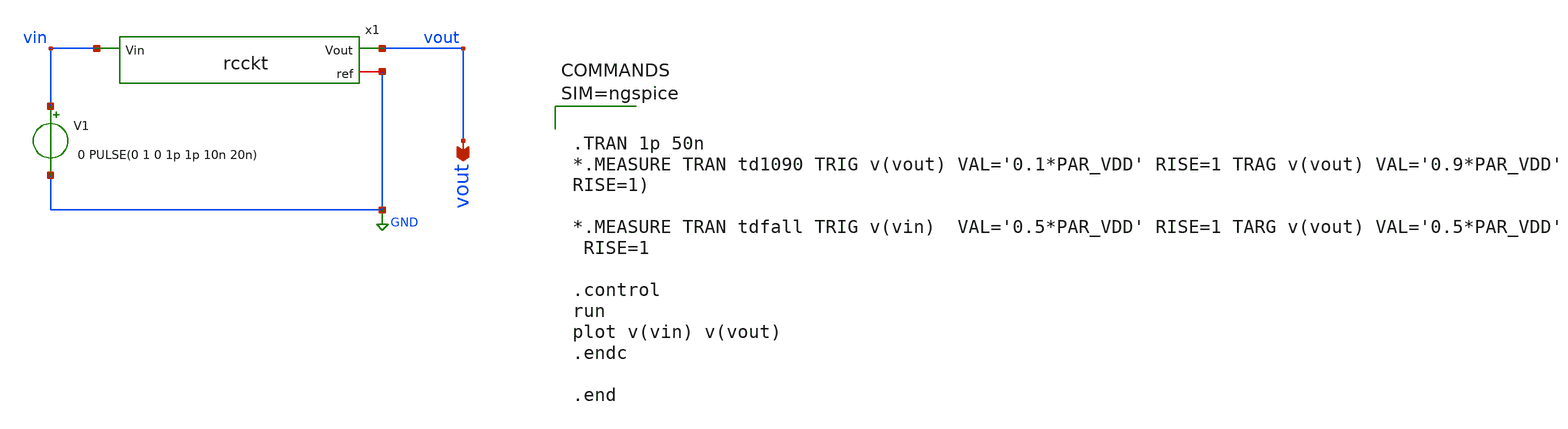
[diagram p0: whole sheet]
** sch_path: xschem/rcckt1.sch
**.subckt rcckt1 vout
*.opin vout
x1 vin vout GND rcckt
V1 vin GND 0 PULSE(0 1 0 1p 1p 10n 20n)
**** begin user architecture code



.TRAN 1p 50n
*.MEASURE TRAN td1090 TRIG v(vout) VAL='0.1*PAR_VDD' RISE=1 TRAG v(vout) VAL='0.9*PAR_VDD'
RISE=1)

*.MEASURE TRAN tdfall TRIG v(vin)  VAL='0.5*PAR_VDD' RISE=1 TARG v(vout) VAL='0.5*PAR_VDD'
 RISE=1

.control
run
plot v(vin) v(vout)
.endc

.end



**** end user architecture code
**.ends
.GLOBAL GND
.end
